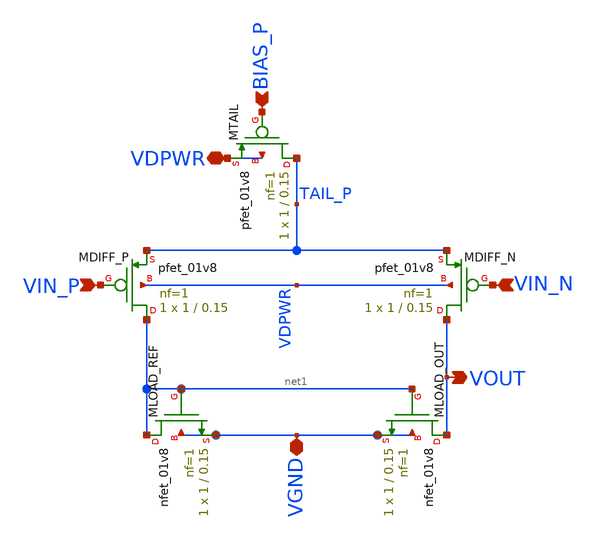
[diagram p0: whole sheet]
** sch_path: xschem/ota_5t.sch
**.subckt ota_5t VIN_P VIN_N BIAS_P VDPWR VGND VOUT
*.ipin VIN_P
*.ipin VIN_N
*.ipin BIAS_P
*.iopin VDPWR
*.iopin VGND
*.opin VOUT
XMDIFF_P net1 VIN_P TAIL_P VDPWR sky130_fd_pr__pfet_01v8 L=0.15 W=1 nf=1 ad='int((1 + 1)/2) * 1 / 1 * 0.29'
+ as='int((1 + 2)/2) * 1 / 1 * 0.29' pd='2*int((1 + 1)/2) * (1 / 1 + 0.29)' ps='2*int((1 + 2)/2) * (1 / 1 + 0.29)'
+ nrd='0.29 / 1 ' nrs='0.29 / 1 ' sa=0 sb=0 sd=0 mult=1 m=1
XMDIFF_N VOUT VIN_N TAIL_P VDPWR sky130_fd_pr__pfet_01v8 L=0.15 W=1 nf=1 ad='int((1 + 1)/2) * 1 / 1 * 0.29'
+ as='int((1 + 2)/2) * 1 / 1 * 0.29' pd='2*int((1 + 1)/2) * (1 / 1 + 0.29)' ps='2*int((1 + 2)/2) * (1 / 1 + 0.29)'
+ nrd='0.29 / 1 ' nrs='0.29 / 1 ' sa=0 sb=0 sd=0 mult=1 m=1
XMTAIL TAIL_P BIAS_P VDPWR VDPWR sky130_fd_pr__pfet_01v8 L=0.15 W=1 nf=1 ad='int((1 + 1)/2) * 1 / 1 * 0.29'
+ as='int((1 + 2)/2) * 1 / 1 * 0.29' pd='2*int((1 + 1)/2) * (1 / 1 + 0.29)' ps='2*int((1 + 2)/2) * (1 / 1 + 0.29)'
+ nrd='0.29 / 1 ' nrs='0.29 / 1 ' sa=0 sb=0 sd=0 mult=1 m=1
XMLOAD_REF net1 net1 VGND VGND sky130_fd_pr__nfet_01v8 L=0.15 W=1 nf=1 ad='int((1 + 1)/2) * 1 / 1 * 0.29'
+ as='int((1 + 2)/2) * 1 / 1 * 0.29' pd='2*int((1 + 1)/2) * (1 / 1 + 0.29)' ps='2*int((1 + 2)/2) * (1 / 1 + 0.29)'
+ nrd='0.29 / 1 ' nrs='0.29 / 1 ' sa=0 sb=0 sd=0 mult=1 m=1
XMLOAD_OUT VOUT net1 VGND VGND sky130_fd_pr__nfet_01v8 L=0.15 W=1 nf=1 ad='int((1 + 1)/2) * 1 / 1 * 0.29'
+ as='int((1 + 2)/2) * 1 / 1 * 0.29' pd='2*int((1 + 1)/2) * (1 / 1 + 0.29)' ps='2*int((1 + 2)/2) * (1 / 1 + 0.29)'
+ nrd='0.29 / 1 ' nrs='0.29 / 1 ' sa=0 sb=0 sd=0 mult=1 m=1
**.ends
.end
